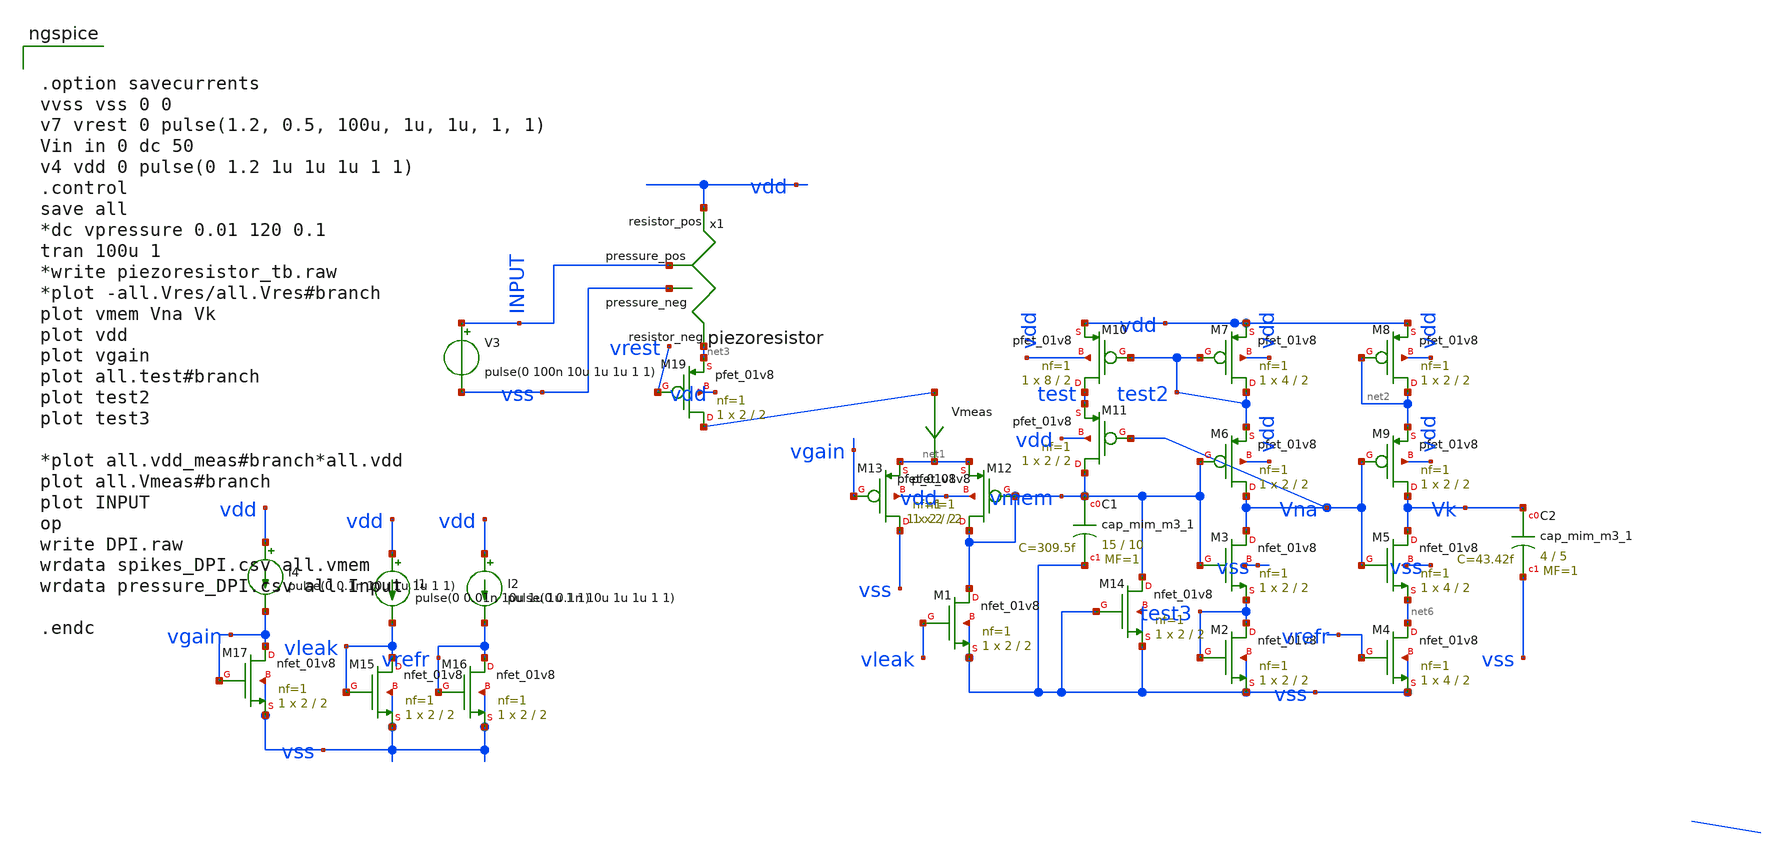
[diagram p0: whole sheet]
** sch_path: circuits/DPI_neuron.sch
* Copyright 2020 Stefan Frederik Schippers
* Licensed under the Apache License, Version 2.0 (the "License");
* you may not use this file except in compliance with the License.
* You may obtain a copy of the License at
* https://www.apache.org/licenses/LICENSE-2.0
* Unless required by applicable law or agreed to in writing, software
* distributed under the License is distributed on an "AS IS" BASIS,
* WITHOUT WARRANTIES OR CONDITIONS OF ANY KIND, either express or implied.
* See the License for the specific language governing permissions and
* limitations under the License.
**.subckt DPI_neuron
Vmeas net4 net1 0
.save i(vmeas)
XM1 vmem vleak vss vss sky130_fd_pr__nfet_01v8 L=2 W=2 nf=1 ad='int((nf+1)/2) * W/nf * 0.29' as='int((nf+2)/2) * W/nf * 0.29'
+ pd='2*int((nf+1)/2) * (W/nf + 0.29)' ps='2*int((nf+2)/2) * (W/nf + 0.29)' nrd='0.29 / W' nrs='0.29 / W'
+ sa=0 sb=0 sd=0 mult=1 m=1
XM2 test3 test3 vss vss sky130_fd_pr__nfet_01v8 L=2 W=2 nf=1 ad='int((nf+1)/2) * W/nf * 0.29' as='int((nf+2)/2) * W/nf * 0.29'
+ pd='2*int((nf+1)/2) * (W/nf + 0.29)' ps='2*int((nf+2)/2) * (W/nf + 0.29)' nrd='0.29 / W' nrs='0.29 / W'
+ sa=0 sb=0 sd=0 mult=1 m=1
XM3 Vna vmem test3 vss sky130_fd_pr__nfet_01v8 L=2 W=2 nf=1 ad='int((nf+1)/2) * W/nf * 0.29' as='int((nf+2)/2) * W/nf * 0.29'
+ pd='2*int((nf+1)/2) * (W/nf + 0.29)' ps='2*int((nf+2)/2) * (W/nf + 0.29)' nrd='0.29 / W' nrs='0.29 / W'
+ sa=0 sb=0 sd=0 mult=1 m=1
XC1 vmem vss sky130_fd_pr__cap_mim_m3_1 W=15 L=10 MF=1 m=1
XC2 Vk vss sky130_fd_pr__cap_mim_m3_1 W=4 L=5 MF=1 m=1
XM14 vmem vss vss vss sky130_fd_pr__nfet_01v8 L=2 W=2 nf=1 ad='int((nf+1)/2) * W/nf * 0.29' as='int((nf+2)/2) * W/nf * 0.29'
+ pd='2*int((nf+1)/2) * (W/nf + 0.29)' ps='2*int((nf+2)/2) * (W/nf + 0.29)' nrd='0.29 / W' nrs='0.29 / W'
+ sa=0 sb=0 sd=0 mult=1 m=1
XM4 net6 vrefr vss vss sky130_fd_pr__nfet_01v8 L=2 W=4 nf=1 ad='int((nf+1)/2) * W/nf * 0.29' as='int((nf+2)/2) * W/nf * 0.29'
+ pd='2*int((nf+1)/2) * (W/nf + 0.29)' ps='2*int((nf+2)/2) * (W/nf + 0.29)' nrd='0.29 / W' nrs='0.29 / W'
+ sa=0 sb=0 sd=0 mult=1 m=1
XM5 Vk Vna net6 vss sky130_fd_pr__nfet_01v8 L=2 W=4 nf=1 ad='int((nf+1)/2) * W/nf * 0.29' as='int((nf+2)/2) * W/nf * 0.29'
+ pd='2*int((nf+1)/2) * (W/nf + 0.29)' ps='2*int((nf+2)/2) * (W/nf + 0.29)' nrd='0.29 / W' nrs='0.29 / W'
+ sa=0 sb=0 sd=0 mult=1 m=1
XM15 vleak vleak vss vss sky130_fd_pr__nfet_01v8 L=2 W=2 nf=1 ad='int((nf+1)/2) * W/nf * 0.29' as='int((nf+2)/2) * W/nf * 0.29'
+ pd='2*int((nf+1)/2) * (W/nf + 0.29)' ps='2*int((nf+2)/2) * (W/nf + 0.29)' nrd='0.29 / W' nrs='0.29 / W'
+ sa=0 sb=0 sd=0 mult=1 m=1
XM16 vrefr vrefr vss vss sky130_fd_pr__nfet_01v8 L=2 W=2 nf=1 ad='int((nf+1)/2) * W/nf * 0.29' as='int((nf+2)/2) * W/nf * 0.29'
+ pd='2*int((nf+1)/2) * (W/nf + 0.29)' ps='2*int((nf+2)/2) * (W/nf + 0.29)' nrd='0.29 / W' nrs='0.29 / W'
+ sa=0 sb=0 sd=0 mult=1 m=1
I4 vdd vgain pulse(0 0.1n 10u 1u 1u 1 1)
XM17 vgain vgain vss vss sky130_fd_pr__nfet_01v8 L=2 W=2 nf=1 ad='int((nf+1)/2) * W/nf * 0.29' as='int((nf+2)/2) * W/nf * 0.29'
+ pd='2*int((nf+1)/2) * (W/nf + 0.29)' ps='2*int((nf+2)/2) * (W/nf + 0.29)' nrd='0.29 / W' nrs='0.29 / W'
+ sa=0 sb=0 sd=0 mult=1 m=1
XM6 Vna vmem test2 vdd sky130_fd_pr__pfet_01v8 L=2 W=2 nf=1 ad='int((nf+1)/2) * W/nf * 0.29' as='int((nf+2)/2) * W/nf * 0.29'
+ pd='2*int((nf+1)/2) * (W/nf + 0.29)' ps='2*int((nf+2)/2) * (W/nf + 0.29)' nrd='0.29 / W' nrs='0.29 / W'
+ sa=0 sb=0 sd=0 mult=1 m=1
XM7 test2 test2 vdd vdd sky130_fd_pr__pfet_01v8 L=2 W=4 nf=1 ad='int((nf+1)/2) * W/nf * 0.29' as='int((nf+2)/2) * W/nf * 0.29'
+ pd='2*int((nf+1)/2) * (W/nf + 0.29)' ps='2*int((nf+2)/2) * (W/nf + 0.29)' nrd='0.29 / W' nrs='0.29 / W'
+ sa=0 sb=0 sd=0 mult=1 m=1
XM8 net2 net2 vdd vdd sky130_fd_pr__pfet_01v8 L=2 W=2 nf=1 ad='int((nf+1)/2) * W/nf * 0.29' as='int((nf+2)/2) * W/nf * 0.29'
+ pd='2*int((nf+1)/2) * (W/nf + 0.29)' ps='2*int((nf+2)/2) * (W/nf + 0.29)' nrd='0.29 / W' nrs='0.29 / W'
+ sa=0 sb=0 sd=0 mult=1 m=1
XM9 Vk Vna net2 vdd sky130_fd_pr__pfet_01v8 L=2 W=2 nf=1 ad='int((nf+1)/2) * W/nf * 0.29' as='int((nf+2)/2) * W/nf * 0.29'
+ pd='2*int((nf+1)/2) * (W/nf + 0.29)' ps='2*int((nf+2)/2) * (W/nf + 0.29)' nrd='0.29 / W' nrs='0.29 / W'
+ sa=0 sb=0 sd=0 mult=1 m=1
XM10 test test2 vdd vdd sky130_fd_pr__pfet_01v8 L=2 W=8 nf=1 ad='int((nf+1)/2) * W/nf * 0.29' as='int((nf+2)/2) * W/nf * 0.29'
+ pd='2*int((nf+1)/2) * (W/nf + 0.29)' ps='2*int((nf+2)/2) * (W/nf + 0.29)' nrd='0.29 / W' nrs='0.29 / W'
+ sa=0 sb=0 sd=0 mult=1 m=1
XM11 vmem Vna test vdd sky130_fd_pr__pfet_01v8 L=2 W=2 nf=1 ad='int((nf+1)/2) * W/nf * 0.29' as='int((nf+2)/2) * W/nf * 0.29'
+ pd='2*int((nf+1)/2) * (W/nf + 0.29)' ps='2*int((nf+2)/2) * (W/nf + 0.29)' nrd='0.29 / W' nrs='0.29 / W'
+ sa=0 sb=0 sd=0 mult=1 m=1
XM12 vmem vmem net1 vdd sky130_fd_pr__pfet_01v8 L=2 W=2 nf=1 ad='int((nf+1)/2) * W/nf * 0.29' as='int((nf+2)/2) * W/nf * 0.29'
+ pd='2*int((nf+1)/2) * (W/nf + 0.29)' ps='2*int((nf+2)/2) * (W/nf + 0.29)' nrd='0.29 / W' nrs='0.29 / W'
+ sa=0 sb=0 sd=0 mult=1 m=1
XM13 vss vgain net1 vdd sky130_fd_pr__pfet_01v8 L=2 W=2 nf=1 ad='int((nf+1)/2) * W/nf * 0.29' as='int((nf+2)/2) * W/nf * 0.29'
+ pd='2*int((nf+1)/2) * (W/nf + 0.29)' ps='2*int((nf+2)/2) * (W/nf + 0.29)' nrd='0.29 / W' nrs='0.29 / W'
+ sa=0 sb=0 sd=0 mult=1 m=1
x1 INPUT vss vdd net3 piezoresistor
XM19 net4 vrest net3 vdd sky130_fd_pr__pfet_01v8 L=2 W=2 nf=1 ad='int((nf+1)/2) * W/nf * 0.29' as='int((nf+2)/2) * W/nf * 0.29'
+ pd='2*int((nf+1)/2) * (W/nf + 0.29)' ps='2*int((nf+2)/2) * (W/nf + 0.29)' nrd='0.29 / W' nrs='0.29 / W'
+ sa=0 sb=0 sd=0 mult=1 m=1
I1 vdd vleak pulse(0 0.01n 10u 1u 1u 1 1)
I2 vdd vrefr pulse(0 0.1n 10u 1u 1u 1 1)
V3 INPUT vss pulse(0 100n 10u 1u 1u 1 1)
**** begin user architecture code


.option savecurrents
vvss vss 0 0
v7 vrest 0 pulse(1.2, 0.5, 100u, 1u, 1u, 1, 1)
Vin in 0 dc 50
v4 vdd 0 pulse(0 1.2 1u 1u 1u 1 1)
.control
save all
*dc vpressure 0.01 120 0.1
tran 100u 1
*write piezoresistor_tb.raw
*plot -all.Vres/all.Vres#branch
plot vmem Vna Vk
plot vdd
plot vgain
plot all.test#branch
plot test2
plot test3

*plot all.vdd_meas#branch*all.vdd
plot all.Vmeas#branch
plot INPUT
op
write DPI.raw
wrdata spikes_DPI.csv all.vmem
wrdata pressure_DPI.csv all.Input

.endc


 .lib $::SKYWATER_MODELS/models/sky130.lib.spice tt

.param mc_mm_switch=0
.param mc_pr_switch=1


**** end user architecture code
**.ends

* expanding   symbol:  /home/mast/Progetti/Telluride2021/sky130_TAC3/circuits/piezoresistor.sym # of
*+ pins=4
** sym_path: circuits/piezoresistor.sym
** sch_path: circuits/piezoresistor.sch
.subckt piezoresistor pressure_pos pressure_neg resistor_pos resistor_neg
*.ipin pressure_pos
*.ipin pressure_neg
*.iopin resistor_pos
*.iopin resistor_neg
Broot sqrtp 0 V = sqrt(v(pressure_pos,pressure_neg))
Bres res 0 V = 106*(50/v(sqrtp)-1)*exp(-0.328*v(sqrtp))+15
Brvar resistor_pos resistor_neg I = V(resistor_pos,resistor_neg)/V(res)
.ends

.end
